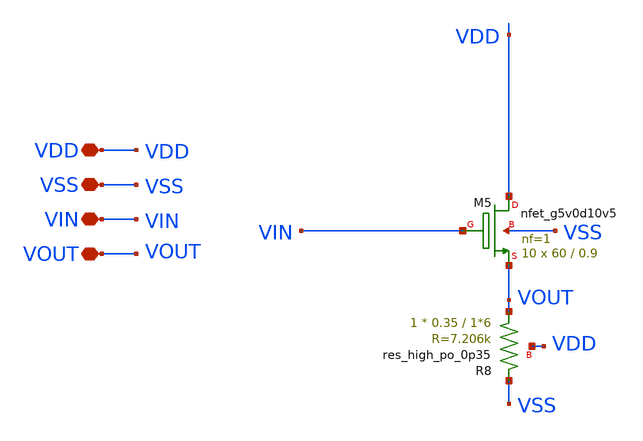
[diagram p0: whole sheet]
** sch_path: amplifiers/single_stage_amps/basic_stages/cd_resistive_stage/cd_resistive_stage.sch
**.subckt cd_resistive_stage VDD VSS VIN VOUT
*.iopin VDD
*.iopin VSS
*.iopin VIN
*.iopin VOUT
XR8 VOUT VSS VDD sky130_fd_pr__res_high_po_0p35 L=1*6 mult=1 m=1
XM5 VDD VIN VOUT VSS sky130_fd_pr__nfet_g5v0d10v5 L=0.9 W=60 nf=1 ad='int((1 + 1)/2) * 60 / 1 * 0.29'
+ as='int((1 + 2)/2) * 60 / 1 * 0.29' pd='2*int((1 + 1)/2) * (60 / 1 + 0.29)' ps='2*int((1 + 2)/2) * (60 / 1 + 0.29)'
+ nrd='0.29 / 60 ' nrs='0.29 / 60 ' sa=0 sb=0 sd=0 mult=10 m=10
**.ends
.end
